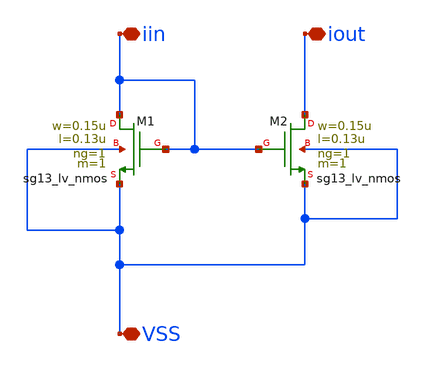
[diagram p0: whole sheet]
** sch_path: analog-db/templates/current_mirror/nmos_current_sink/basic_current_mirror.sch
**.subckt basic_current_mirror VSS iin iout
*.iopin VSS
*.iopin iin
*.iopin iout
XM1 iin iin VSS VSS sg13_lv_nmos w=0.15u l=0.13u ng=1 m=1 mm_ok=1
XM2 iout iin VSS VSS sg13_lv_nmos w=0.15u l=0.13u ng=1 m=1 mm_ok=1
**.ends
.end
